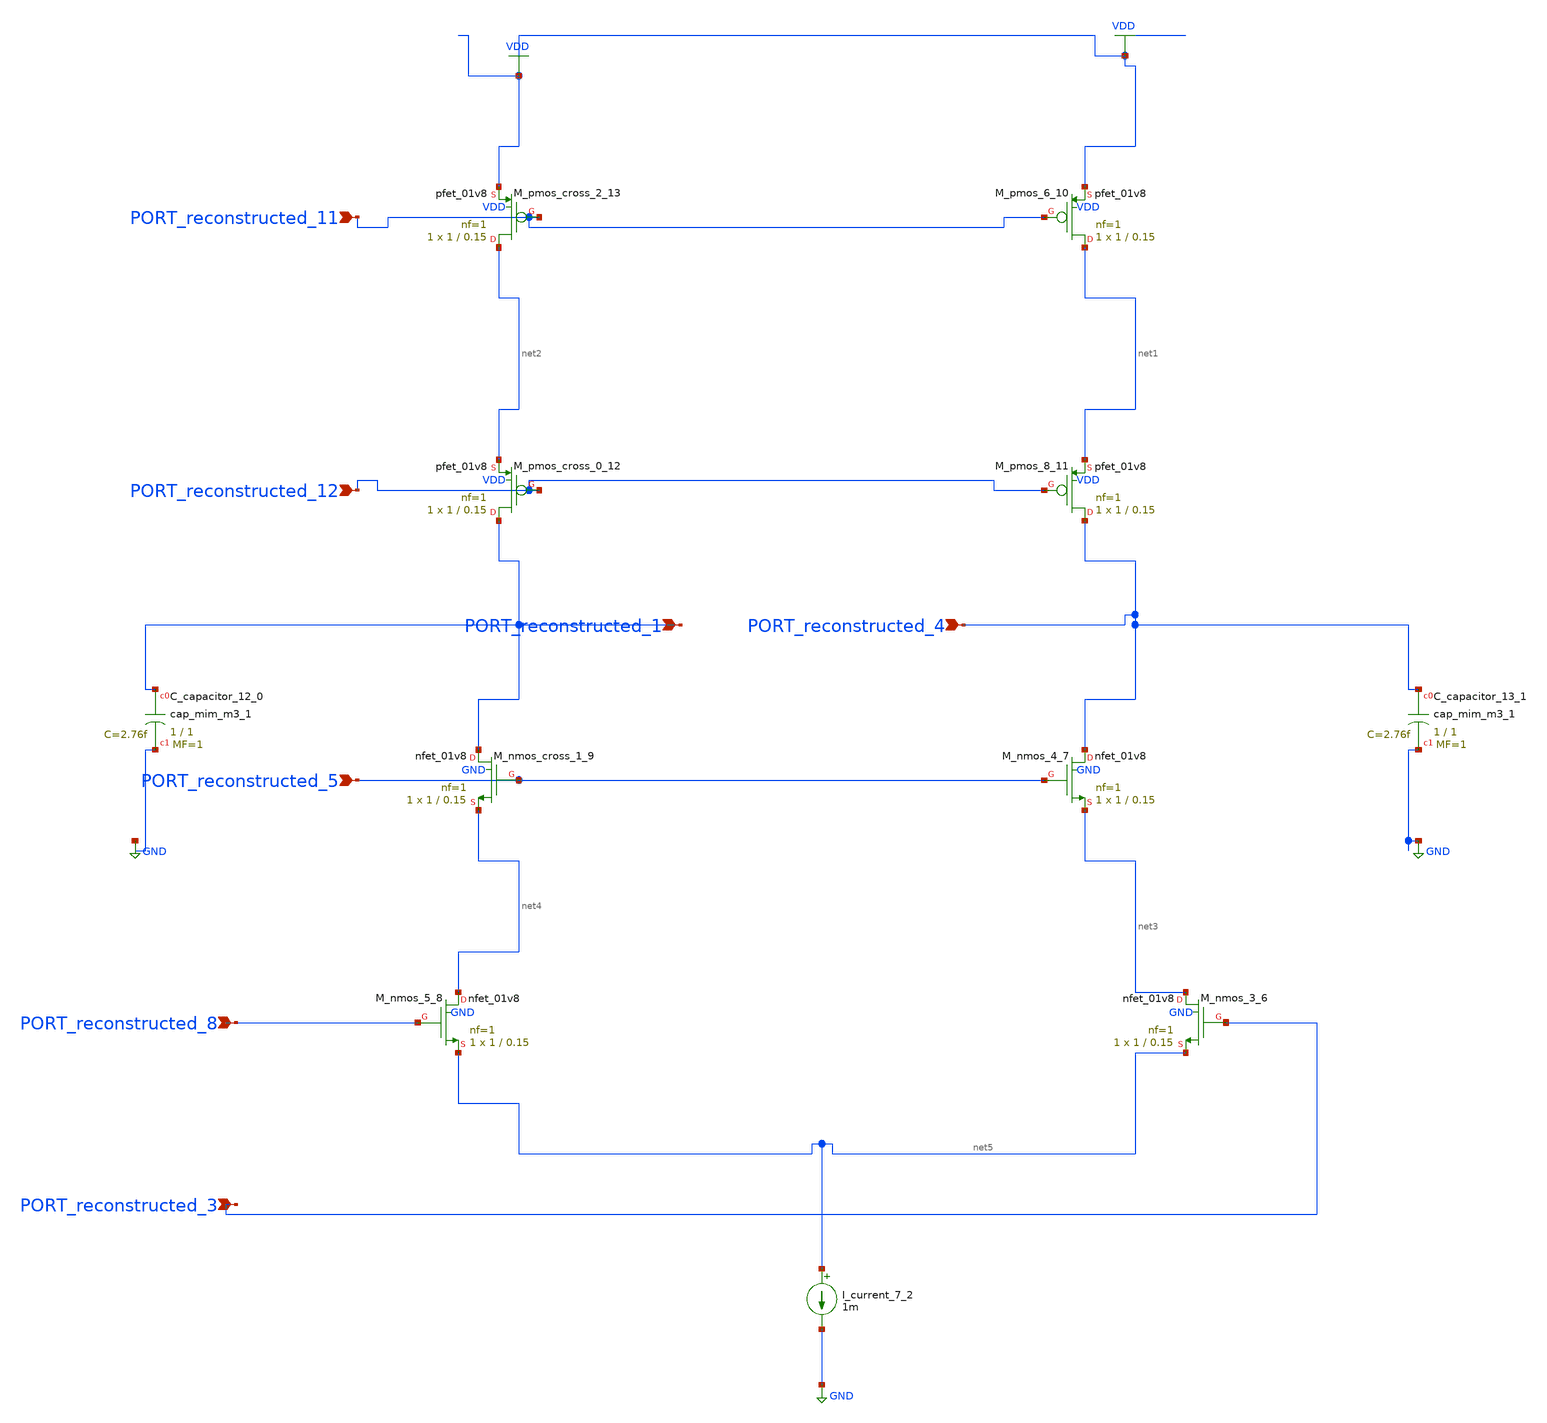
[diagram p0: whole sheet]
** sch_path: schematics/AMSNet/692.sch
**.subckt 692 PORT_reconstructed_1 PORT_reconstructed_4 PORT_reconstructed_8 PORT_reconstructed_3
*+ PORT_reconstructed_5 PORT_reconstructed_12 PORT_reconstructed_11
*.ipin PORT_reconstructed_1
*.ipin PORT_reconstructed_4
*.ipin PORT_reconstructed_8
*.ipin PORT_reconstructed_3
*.ipin PORT_reconstructed_5
*.ipin PORT_reconstructed_12
*.ipin PORT_reconstructed_11
XC_capacitor_12_0 PORT_reconstructed_1 GND sky130_fd_pr__cap_mim_m3_1 W=1 L=1 MF=1 m=1
XC_capacitor_13_1 PORT_reconstructed_4 GND sky130_fd_pr__cap_mim_m3_1 W=1 L=1 MF=1 m=1
I_current_7_2 net5 GND 1m
XM_nmos_3_6 net3 PORT_reconstructed_3 net5 GND sky130_fd_pr__nfet_01v8 L=0.15 W=1 nf=1 ad='int((1 + 1)/2) * 1 / 1 * 0.29'
+ as='int((1 + 2)/2) * 1 / 1 * 0.29' pd='2*int((1 + 1)/2) * (1 / 1 + 0.29)' ps='2*int((1 + 2)/2) * (1 / 1 + 0.29)'
+ nrd='0.29 / 1 ' nrs='0.29 / 1 ' sa=0 sb=0 sd=0 mult=1 m=1
XM_nmos_4_7 PORT_reconstructed_4 PORT_reconstructed_5 net3 GND sky130_fd_pr__nfet_01v8 L=0.15 W=1 nf=1
+ ad='int((1 + 1)/2) * 1 / 1 * 0.29' as='int((1 + 2)/2) * 1 / 1 * 0.29' pd='2*int((1 + 1)/2) * (1 / 1 + 0.29)'
+ ps='2*int((1 + 2)/2) * (1 / 1 + 0.29)' nrd='0.29 / 1 ' nrs='0.29 / 1 ' sa=0 sb=0 sd=0 mult=1 m=1
XM_nmos_5_8 net4 PORT_reconstructed_8 net5 GND sky130_fd_pr__nfet_01v8 L=0.15 W=1 nf=1 ad='int((1 + 1)/2) * 1 / 1 * 0.29'
+ as='int((1 + 2)/2) * 1 / 1 * 0.29' pd='2*int((1 + 1)/2) * (1 / 1 + 0.29)' ps='2*int((1 + 2)/2) * (1 / 1 + 0.29)'
+ nrd='0.29 / 1 ' nrs='0.29 / 1 ' sa=0 sb=0 sd=0 mult=1 m=1
XM_nmos_cross_1_9 PORT_reconstructed_1 PORT_reconstructed_5 net4 GND sky130_fd_pr__nfet_01v8 L=0.15 W=1
+ nf=1 ad='int((1 + 1)/2) * 1 / 1 * 0.29' as='int((1 + 2)/2) * 1 / 1 * 0.29' pd='2*int((1 + 1)/2) * (1 / 1 + 0.29)'
+ ps='2*int((1 + 2)/2) * (1 / 1 + 0.29)' nrd='0.29 / 1 ' nrs='0.29 / 1 ' sa=0 sb=0 sd=0 mult=1 m=1
XM_pmos_6_10 net1 PORT_reconstructed_11 VDD VDD sky130_fd_pr__pfet_01v8 L=0.15 W=1 nf=1 ad='int((1 + 1)/2) * 1 / 1 * 0.29'
+ as='int((1 + 2)/2) * 1 / 1 * 0.29' pd='2*int((1 + 1)/2) * (1 / 1 + 0.29)' ps='2*int((1 + 2)/2) * (1 / 1 + 0.29)'
+ nrd='0.29 / 1 ' nrs='0.29 / 1 ' sa=0 sb=0 sd=0 mult=1 m=1
XM_pmos_8_11 PORT_reconstructed_4 PORT_reconstructed_12 net1 VDD sky130_fd_pr__pfet_01v8 L=0.15 W=1 nf=1
+ ad='int((1 + 1)/2) * 1 / 1 * 0.29' as='int((1 + 2)/2) * 1 / 1 * 0.29' pd='2*int((1 + 1)/2) * (1 / 1 + 0.29)'
+ ps='2*int((1 + 2)/2) * (1 / 1 + 0.29)' nrd='0.29 / 1 ' nrs='0.29 / 1 ' sa=0 sb=0 sd=0 mult=1 m=1
XM_pmos_cross_0_12 PORT_reconstructed_1 PORT_reconstructed_12 net2 VDD sky130_fd_pr__pfet_01v8 L=0.15
+ W=1 nf=1 ad='int((1 + 1)/2) * 1 / 1 * 0.29' as='int((1 + 2)/2) * 1 / 1 * 0.29' pd='2*int((1 + 1)/2) * (1 / 1 + 0.29)'
+ ps='2*int((1 + 2)/2) * (1 / 1 + 0.29)' nrd='0.29 / 1 ' nrs='0.29 / 1 ' sa=0 sb=0 sd=0 mult=1 m=1
XM_pmos_cross_2_13 net2 PORT_reconstructed_11 VDD VDD sky130_fd_pr__pfet_01v8 L=0.15 W=1 nf=1 ad='int((1 + 1)/2) * 1 / 1 * 0.29'
+ as='int((1 + 2)/2) * 1 / 1 * 0.29' pd='2*int((1 + 1)/2) * (1 / 1 + 0.29)' ps='2*int((1 + 2)/2) * (1 / 1 + 0.29)'
+ nrd='0.29 / 1 ' nrs='0.29 / 1 ' sa=0 sb=0 sd=0 mult=1 m=1
**.ends
.GLOBAL GND
.GLOBAL VDD
.end
